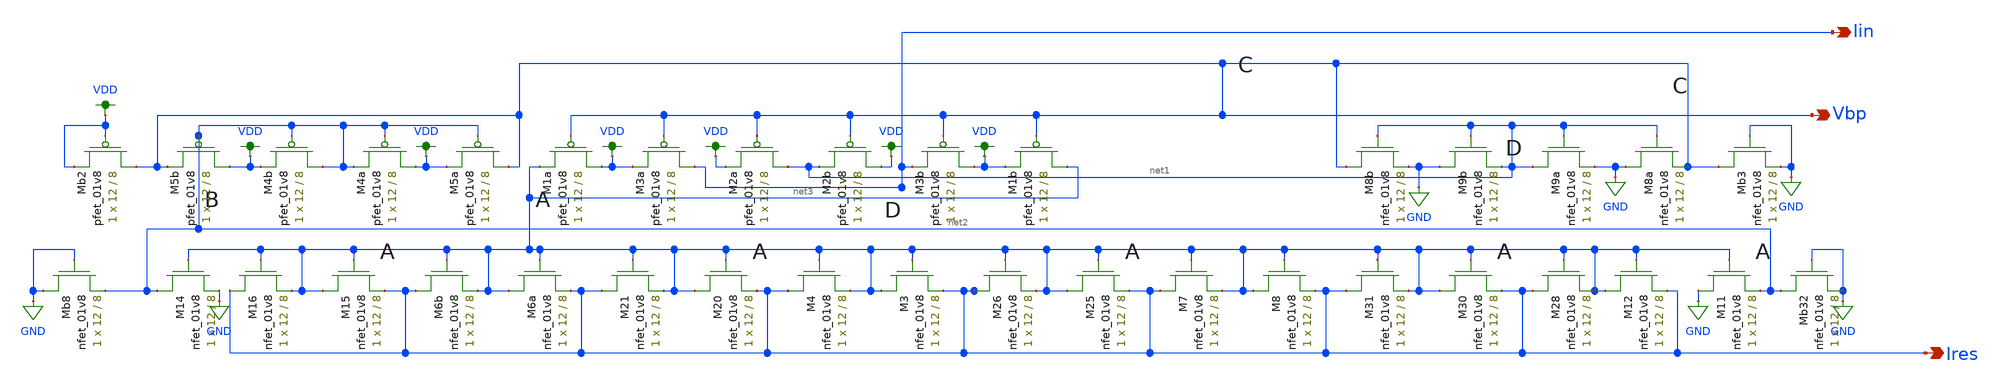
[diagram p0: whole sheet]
** sch_path: xschem/curgen_lds.sch
**.subckt curgen_lds Iin Vbp Ires
*.opin Iin
*.opin Vbp
*.opin Ires
XM3b VDD Vbp Iin VDD sky130_fd_pr__pfet_01v8 L=8 W=12 nf=1 ad='int((nf+1)/2) * W/nf * 0.29' as='int((nf+2)/2) * W/nf * 0.29'
+ pd='2*int((nf+1)/2) * (W/nf + 0.29)' ps='2*int((nf+2)/2) * (W/nf + 0.29)' nrd='0.29 / W' nrs='0.29 / W'
+ sa=0 sb=0 sd=0 mult=1 m=1
XM3a Iin Vbp VDD VDD sky130_fd_pr__pfet_01v8 L=8 W=12 nf=1 ad='int((nf+1)/2) * W/nf * 0.29' as='int((nf+2)/2) * W/nf * 0.29'
+ pd='2*int((nf+1)/2) * (W/nf + 0.29)' ps='2*int((nf+2)/2) * (W/nf + 0.29)' nrd='0.29 / W' nrs='0.29 / W'
+ sa=0 sb=0 sd=0 mult=1 m=1
XM2b VDD Vbp net1 VDD sky130_fd_pr__pfet_01v8 L=8 W=12 nf=1 ad='int((nf+1)/2) * W/nf * 0.29' as='int((nf+2)/2) * W/nf * 0.29'
+ pd='2*int((nf+1)/2) * (W/nf + 0.29)' ps='2*int((nf+2)/2) * (W/nf + 0.29)' nrd='0.29 / W' nrs='0.29 / W'
+ sa=0 sb=0 sd=0 mult=1 m=1
XM2a net1 Vbp VDD VDD sky130_fd_pr__pfet_01v8 L=8 W=12 nf=1 ad='int((nf+1)/2) * W/nf * 0.29' as='int((nf+2)/2) * W/nf * 0.29'
+ pd='2*int((nf+1)/2) * (W/nf + 0.29)' ps='2*int((nf+2)/2) * (W/nf + 0.29)' nrd='0.29 / W' nrs='0.29 / W'
+ sa=0 sb=0 sd=0 mult=1 m=1
XM1b net3 Vbp VDD VDD sky130_fd_pr__pfet_01v8 L=8 W=12 nf=1 ad='int((nf+1)/2) * W/nf * 0.29' as='int((nf+2)/2) * W/nf * 0.29'
+ pd='2*int((nf+1)/2) * (W/nf + 0.29)' ps='2*int((nf+2)/2) * (W/nf + 0.29)' nrd='0.29 / W' nrs='0.29 / W'
+ sa=0 sb=0 sd=0 mult=1 m=1
XM1a VDD Vbp net3 VDD sky130_fd_pr__pfet_01v8 L=8 W=12 nf=1 ad='int((nf+1)/2) * W/nf * 0.29' as='int((nf+2)/2) * W/nf * 0.29'
+ pd='2*int((nf+1)/2) * (W/nf + 0.29)' ps='2*int((nf+2)/2) * (W/nf + 0.29)' nrd='0.29 / W' nrs='0.29 / W'
+ sa=0 sb=0 sd=0 mult=1 m=1
XM4b net2 net2 VDD VDD sky130_fd_pr__pfet_01v8 L=8 W=12 nf=1 ad='int((nf+1)/2) * W/nf * 0.29' as='int((nf+2)/2) * W/nf * 0.29'
+ pd='2*int((nf+1)/2) * (W/nf + 0.29)' ps='2*int((nf+2)/2) * (W/nf + 0.29)' nrd='0.29 / W' nrs='0.29 / W'
+ sa=0 sb=0 sd=0 mult=1 m=1
XM4a VDD net2 net2 VDD sky130_fd_pr__pfet_01v8 L=8 W=12 nf=1 ad='int((nf+1)/2) * W/nf * 0.29' as='int((nf+2)/2) * W/nf * 0.29'
+ pd='2*int((nf+1)/2) * (W/nf + 0.29)' ps='2*int((nf+2)/2) * (W/nf + 0.29)' nrd='0.29 / W' nrs='0.29 / W'
+ sa=0 sb=0 sd=0 mult=1 m=1
XM5a Vbp net2 VDD VDD sky130_fd_pr__pfet_01v8 L=8 W=12 nf=1 ad='int((nf+1)/2) * W/nf * 0.29' as='int((nf+2)/2) * W/nf * 0.29'
+ pd='2*int((nf+1)/2) * (W/nf + 0.29)' ps='2*int((nf+2)/2) * (W/nf + 0.29)' nrd='0.29 / W' nrs='0.29 / W'
+ sa=0 sb=0 sd=0 mult=1 m=1
XM5b VDD net2 Vbp VDD sky130_fd_pr__pfet_01v8 L=8 W=12 nf=1 ad='int((nf+1)/2) * W/nf * 0.29' as='int((nf+2)/2) * W/nf * 0.29'
+ pd='2*int((nf+1)/2) * (W/nf + 0.29)' ps='2*int((nf+2)/2) * (W/nf + 0.29)' nrd='0.29 / W' nrs='0.29 / W'
+ sa=0 sb=0 sd=0 mult=1 m=1
XMb2 Vbp VDD VDD VDD sky130_fd_pr__pfet_01v8 L=8 W=12 nf=1 ad='int((nf+1)/2) * W/nf * 0.29' as='int((nf+2)/2) * W/nf * 0.29'
+ pd='2*int((nf+1)/2) * (W/nf + 0.29)' ps='2*int((nf+2)/2) * (W/nf + 0.29)' nrd='0.29 / W' nrs='0.29 / W'
+ sa=0 sb=0 sd=0 mult=1 m=1
XM8a GND net1 Vbp GND sky130_fd_pr__nfet_01v8 L=8 W=12 nf=1 ad='int((nf+1)/2) * W/nf * 0.29' as='int((nf+2)/2) * W/nf * 0.29'
+ pd='2*int((nf+1)/2) * (W/nf + 0.29)' ps='2*int((nf+2)/2) * (W/nf + 0.29)' nrd='0.29 / W' nrs='0.29 / W'
+ sa=0 sb=0 sd=0 mult=1 m=1
XM8b Vbp net1 GND GND sky130_fd_pr__nfet_01v8 L=8 W=12 nf=1 ad='int((nf+1)/2) * W/nf * 0.29' as='int((nf+2)/2) * W/nf * 0.29'
+ pd='2*int((nf+1)/2) * (W/nf + 0.29)' ps='2*int((nf+2)/2) * (W/nf + 0.29)' nrd='0.29 / W' nrs='0.29 / W'
+ sa=0 sb=0 sd=0 mult=1 m=1
XM9a net1 net1 GND GND sky130_fd_pr__nfet_01v8 L=8 W=12 nf=1 ad='int((nf+1)/2) * W/nf * 0.29' as='int((nf+2)/2) * W/nf * 0.29'
+ pd='2*int((nf+1)/2) * (W/nf + 0.29)' ps='2*int((nf+2)/2) * (W/nf + 0.29)' nrd='0.29 / W' nrs='0.29 / W'
+ sa=0 sb=0 sd=0 mult=1 m=1
XM9b GND net1 net1 GND sky130_fd_pr__nfet_01v8 L=8 W=12 nf=1 ad='int((nf+1)/2) * W/nf * 0.29' as='int((nf+2)/2) * W/nf * 0.29'
+ pd='2*int((nf+1)/2) * (W/nf + 0.29)' ps='2*int((nf+2)/2) * (W/nf + 0.29)' nrd='0.29 / W' nrs='0.29 / W'
+ sa=0 sb=0 sd=0 mult=1 m=1
XMb3 Vbp GND GND GND sky130_fd_pr__nfet_01v8 L=8 W=12 nf=1 ad='int((nf+1)/2) * W/nf * 0.29' as='int((nf+2)/2) * W/nf * 0.29'
+ pd='2*int((nf+1)/2) * (W/nf + 0.29)' ps='2*int((nf+2)/2) * (W/nf + 0.29)' nrd='0.29 / W' nrs='0.29 / W'
+ sa=0 sb=0 sd=0 mult=1 m=1
XM6a net3 net3 Ires GND sky130_fd_pr__nfet_01v8 L=8 W=12 nf=1 ad='int((nf+1)/2) * W/nf * 0.29' as='int((nf+2)/2) * W/nf * 0.29'
+ pd='2*int((nf+1)/2) * (W/nf + 0.29)' ps='2*int((nf+2)/2) * (W/nf + 0.29)' nrd='0.29 / W' nrs='0.29 / W'
+ sa=0 sb=0 sd=0 mult=1 m=1
XM3 net3 net3 Ires GND sky130_fd_pr__nfet_01v8 L=8 W=12 nf=1 ad='int((nf+1)/2) * W/nf * 0.29' as='int((nf+2)/2) * W/nf * 0.29'
+ pd='2*int((nf+1)/2) * (W/nf + 0.29)' ps='2*int((nf+2)/2) * (W/nf + 0.29)' nrd='0.29 / W' nrs='0.29 / W'
+ sa=0 sb=0 sd=0 mult=1 m=1
XM4 Ires net3 net3 GND sky130_fd_pr__nfet_01v8 L=8 W=12 nf=1 ad='int((nf+1)/2) * W/nf * 0.29' as='int((nf+2)/2) * W/nf * 0.29'
+ pd='2*int((nf+1)/2) * (W/nf + 0.29)' ps='2*int((nf+2)/2) * (W/nf + 0.29)' nrd='0.29 / W' nrs='0.29 / W'
+ sa=0 sb=0 sd=0 mult=1 m=1
XM7 Ires net3 net3 GND sky130_fd_pr__nfet_01v8 L=8 W=12 nf=1 ad='int((nf+1)/2) * W/nf * 0.29' as='int((nf+2)/2) * W/nf * 0.29'
+ pd='2*int((nf+1)/2) * (W/nf + 0.29)' ps='2*int((nf+2)/2) * (W/nf + 0.29)' nrd='0.29 / W' nrs='0.29 / W'
+ sa=0 sb=0 sd=0 mult=1 m=1
XM8 net3 net3 Ires GND sky130_fd_pr__nfet_01v8 L=8 W=12 nf=1 ad='int((nf+1)/2) * W/nf * 0.29' as='int((nf+2)/2) * W/nf * 0.29'
+ pd='2*int((nf+1)/2) * (W/nf + 0.29)' ps='2*int((nf+2)/2) * (W/nf + 0.29)' nrd='0.29 / W' nrs='0.29 / W'
+ sa=0 sb=0 sd=0 mult=1 m=1
XM11 GND net3 net2 GND sky130_fd_pr__nfet_01v8 L=8 W=12 nf=1 ad='int((nf+1)/2) * W/nf * 0.29' as='int((nf+2)/2) * W/nf * 0.29'
+ pd='2*int((nf+1)/2) * (W/nf + 0.29)' ps='2*int((nf+2)/2) * (W/nf + 0.29)' nrd='0.29 / W' nrs='0.29 / W'
+ sa=0 sb=0 sd=0 mult=1 m=1
XM12 net3 net3 Ires GND sky130_fd_pr__nfet_01v8 L=8 W=12 nf=1 ad='int((nf+1)/2) * W/nf * 0.29' as='int((nf+2)/2) * W/nf * 0.29'
+ pd='2*int((nf+1)/2) * (W/nf + 0.29)' ps='2*int((nf+2)/2) * (W/nf + 0.29)' nrd='0.29 / W' nrs='0.29 / W'
+ sa=0 sb=0 sd=0 mult=1 m=1
XMb8 GND GND net2 GND sky130_fd_pr__nfet_01v8 L=8 W=12 nf=1 ad='int((nf+1)/2) * W/nf * 0.29' as='int((nf+2)/2) * W/nf * 0.29'
+ pd='2*int((nf+1)/2) * (W/nf + 0.29)' ps='2*int((nf+2)/2) * (W/nf + 0.29)' nrd='0.29 / W' nrs='0.29 / W'
+ sa=0 sb=0 sd=0 mult=1 m=1
XM14 net2 net3 GND GND sky130_fd_pr__nfet_01v8 L=8 W=12 nf=1 ad='int((nf+1)/2) * W/nf * 0.29' as='int((nf+2)/2) * W/nf * 0.29'
+ pd='2*int((nf+1)/2) * (W/nf + 0.29)' ps='2*int((nf+2)/2) * (W/nf + 0.29)' nrd='0.29 / W' nrs='0.29 / W'
+ sa=0 sb=0 sd=0 mult=1 m=1
XM15 net3 net3 Ires GND sky130_fd_pr__nfet_01v8 L=8 W=12 nf=1 ad='int((nf+1)/2) * W/nf * 0.29' as='int((nf+2)/2) * W/nf * 0.29'
+ pd='2*int((nf+1)/2) * (W/nf + 0.29)' ps='2*int((nf+2)/2) * (W/nf + 0.29)' nrd='0.29 / W' nrs='0.29 / W'
+ sa=0 sb=0 sd=0 mult=1 m=1
XM16 Ires net3 net3 GND sky130_fd_pr__nfet_01v8 L=8 W=12 nf=1 ad='int((nf+1)/2) * W/nf * 0.29' as='int((nf+2)/2) * W/nf * 0.29'
+ pd='2*int((nf+1)/2) * (W/nf + 0.29)' ps='2*int((nf+2)/2) * (W/nf + 0.29)' nrd='0.29 / W' nrs='0.29 / W'
+ sa=0 sb=0 sd=0 mult=1 m=1
XM20 net3 net3 Ires GND sky130_fd_pr__nfet_01v8 L=8 W=12 nf=1 ad='int((nf+1)/2) * W/nf * 0.29' as='int((nf+2)/2) * W/nf * 0.29'
+ pd='2*int((nf+1)/2) * (W/nf + 0.29)' ps='2*int((nf+2)/2) * (W/nf + 0.29)' nrd='0.29 / W' nrs='0.29 / W'
+ sa=0 sb=0 sd=0 mult=1 m=1
XM21 Ires net3 net3 GND sky130_fd_pr__nfet_01v8 L=8 W=12 nf=1 ad='int((nf+1)/2) * W/nf * 0.29' as='int((nf+2)/2) * W/nf * 0.29'
+ pd='2*int((nf+1)/2) * (W/nf + 0.29)' ps='2*int((nf+2)/2) * (W/nf + 0.29)' nrd='0.29 / W' nrs='0.29 / W'
+ sa=0 sb=0 sd=0 mult=1 m=1
XM25 net3 net3 Ires GND sky130_fd_pr__nfet_01v8 L=8 W=12 nf=1 ad='int((nf+1)/2) * W/nf * 0.29' as='int((nf+2)/2) * W/nf * 0.29'
+ pd='2*int((nf+1)/2) * (W/nf + 0.29)' ps='2*int((nf+2)/2) * (W/nf + 0.29)' nrd='0.29 / W' nrs='0.29 / W'
+ sa=0 sb=0 sd=0 mult=1 m=1
XM26 Ires net3 net3 GND sky130_fd_pr__nfet_01v8 L=8 W=12 nf=1 ad='int((nf+1)/2) * W/nf * 0.29' as='int((nf+2)/2) * W/nf * 0.29'
+ pd='2*int((nf+1)/2) * (W/nf + 0.29)' ps='2*int((nf+2)/2) * (W/nf + 0.29)' nrd='0.29 / W' nrs='0.29 / W'
+ sa=0 sb=0 sd=0 mult=1 m=1
XM28 Ires net3 net3 GND sky130_fd_pr__nfet_01v8 L=8 W=12 nf=1 ad='int((nf+1)/2) * W/nf * 0.29' as='int((nf+2)/2) * W/nf * 0.29'
+ pd='2*int((nf+1)/2) * (W/nf + 0.29)' ps='2*int((nf+2)/2) * (W/nf + 0.29)' nrd='0.29 / W' nrs='0.29 / W'
+ sa=0 sb=0 sd=0 mult=1 m=1
XM30 net3 net3 Ires GND sky130_fd_pr__nfet_01v8 L=8 W=12 nf=1 ad='int((nf+1)/2) * W/nf * 0.29' as='int((nf+2)/2) * W/nf * 0.29'
+ pd='2*int((nf+1)/2) * (W/nf + 0.29)' ps='2*int((nf+2)/2) * (W/nf + 0.29)' nrd='0.29 / W' nrs='0.29 / W'
+ sa=0 sb=0 sd=0 mult=1 m=1
XM31 Ires net3 net3 GND sky130_fd_pr__nfet_01v8 L=8 W=12 nf=1 ad='int((nf+1)/2) * W/nf * 0.29' as='int((nf+2)/2) * W/nf * 0.29'
+ pd='2*int((nf+1)/2) * (W/nf + 0.29)' ps='2*int((nf+2)/2) * (W/nf + 0.29)' nrd='0.29 / W' nrs='0.29 / W'
+ sa=0 sb=0 sd=0 mult=1 m=1
XMb32 net2 GND GND GND sky130_fd_pr__nfet_01v8 L=8 W=12 nf=1 ad='int((nf+1)/2) * W/nf * 0.29' as='int((nf+2)/2) * W/nf * 0.29'
+ pd='2*int((nf+1)/2) * (W/nf + 0.29)' ps='2*int((nf+2)/2) * (W/nf + 0.29)' nrd='0.29 / W' nrs='0.29 / W'
+ sa=0 sb=0 sd=0 mult=1 m=1
XM6b Ires net3 net3 GND sky130_fd_pr__nfet_01v8 L=8 W=12 nf=1 ad='int((nf+1)/2) * W/nf * 0.29' as='int((nf+2)/2) * W/nf * 0.29'
+ pd='2*int((nf+1)/2) * (W/nf + 0.29)' ps='2*int((nf+2)/2) * (W/nf + 0.29)' nrd='0.29 / W' nrs='0.29 / W'
+ sa=0 sb=0 sd=0 mult=1 m=1
**.ends
.GLOBAL VDD
.GLOBAL GND
.end
